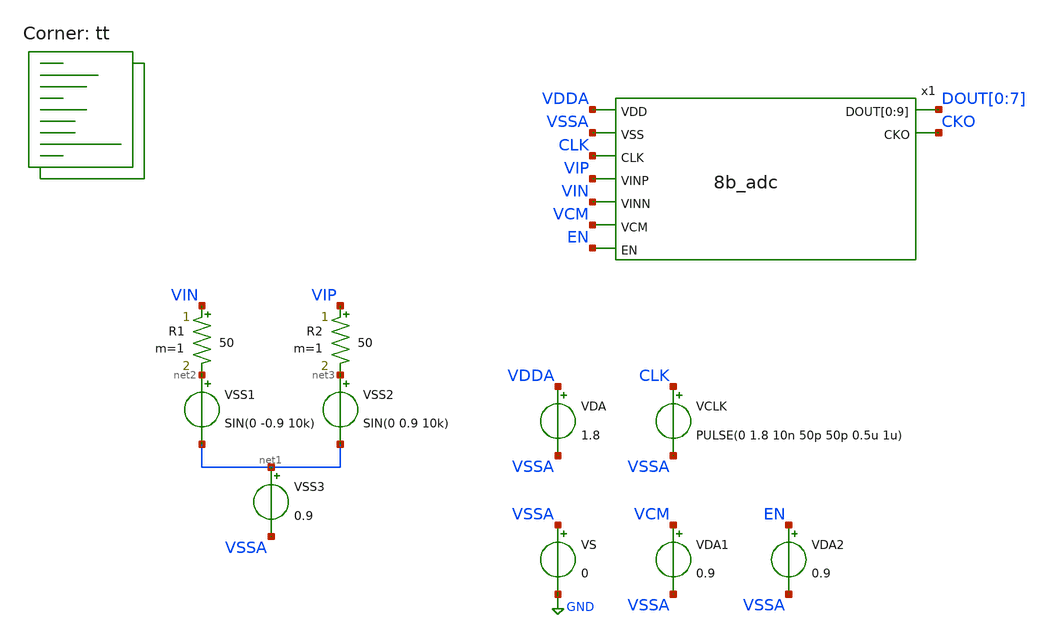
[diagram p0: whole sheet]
** sch_path: xschem/adc_tb.sch
**.subckt adc_tb
VS VSSA GND 0
VDA VDDA VSSA 1.8
VSS1 net2 net1 SIN(0 -0.9 10k)
VSS2 net3 net1 SIN(0 0.9 10k)
VSS3 net1 VSSA 0.9
VCLK CLK VSSA PULSE(0 1.8 10n 50p 50p 0.5u 1u)
R1 VIN net2 50 m=1
R2 VIP net3 50 m=1
x1 VDDA VSSA CLK VIP VIN VCM EN DOUT[0] DOUT[1] DOUT[2] DOUT[3] DOUT[4] DOUT[5] DOUT[6] DOUT[7]
+ DOUT[0] DOUT[1] CKO 8b_adc
VDA1 VCM VSSA 0.9
VDA2 EN VSSA 0.9
**** begin user architecture code

** opencircuitdesign pdks install
* .lib $::SKYWATER_MODELS/sky130.lib.spice tt
.include $PDK_ROOT/$PDK/libs.ref/sky130_fd_sc_hd/spice/sky130_fd_sc_hd.spice



.option wnflag=0
.option savecurrents
.options method=trapezoid
.options solver=iterative
.control
global netlist_dir .
set wr_singlescale
save x1.vcp x1.vcn vip vin clk 'dout[0]' 'dout[1]' 'dout[2]' 'dout[3]' 'dout[4]' 'dout[5]' 'dout[6]'
+ 'dout[7]'  vcm cko x1.cmp_p x1.cmp_n x1.cks x1.cksb  'x1.cf[0]' 'x1.cf[1]' 'x1.cf[2]' 'x1.cf[3]' 'x1.cf[4]'
+ 'x1.cf[5]' 'x1.cf[6]' 'x1.cf[7]'  'x1.swn[0]' 'x1.swn[1]' 'x1.swn[2]' 'x1.swn[3]' 'x1.swn[4]' 'x1.swn[5]'
+ 'x1.swn[6]' 'x1.swn[7]'
tran 10n 0.1m  ; Mengubah start time menjadi 1n
remzerovec
write adc8b_tb.raw
quit 1
.endc

.lib $::SKYWATER_MODELS/sky130.lib.spice tt
**** end user architecture code
**.ends
.GLOBAL GND
.end
